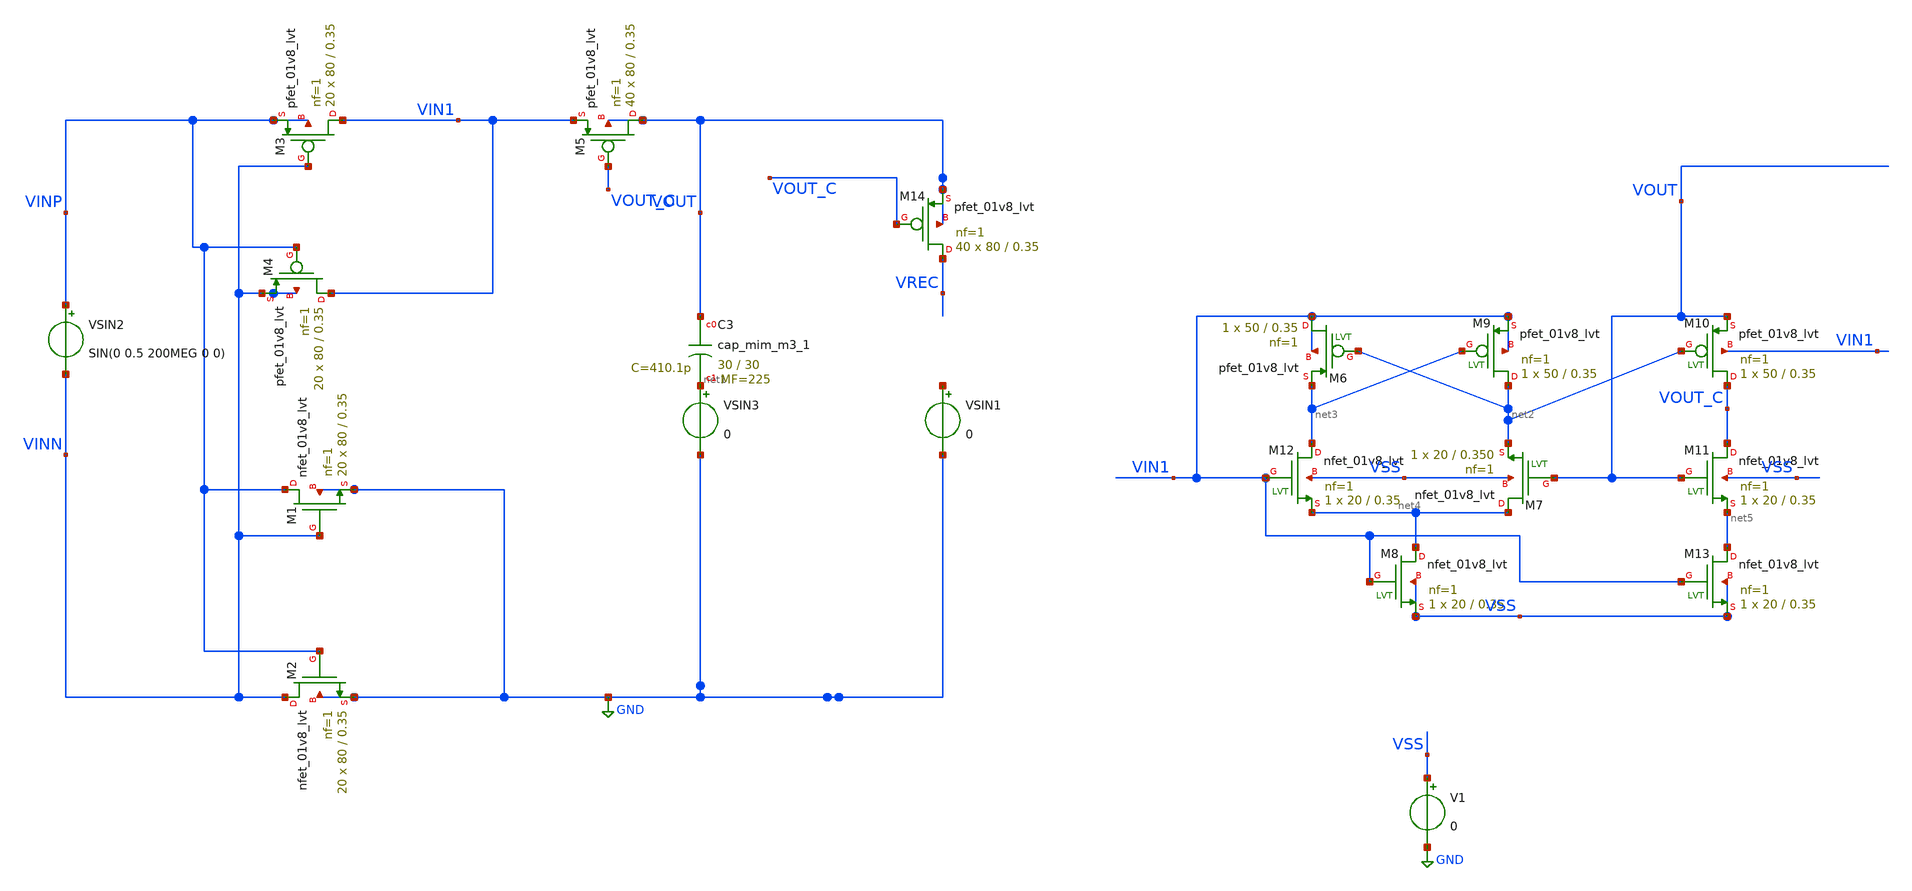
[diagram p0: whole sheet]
** sch_path: Schematics/PICOOAYOUT.sch
**.subckt PICOOAYOUT
XM1 VINP VINN GND GND sky130_fd_pr__nfet_01v8_lvt L=0.35 W=80 nf=1 ad='int((nf+1)/2) * W/nf * 0.29' as='int((nf+2)/2) * W/nf * 0.29'
+ pd='2*int((nf+1)/2) * (W/nf + 0.29)' ps='2*int((nf+2)/2) * (W/nf + 0.29)' nrd='0.29 / W' nrs='0.29 / W'
+ sa=0 sb=0 sd=0 mult=20 m=20
XM2 VINN VINP GND GND sky130_fd_pr__nfet_01v8_lvt L=0.35 W=80 nf=1 ad='int((nf+1)/2) * W/nf * 0.29' as='int((nf+2)/2) * W/nf * 0.29'
+ pd='2*int((nf+1)/2) * (W/nf + 0.29)' ps='2*int((nf+2)/2) * (W/nf + 0.29)' nrd='0.29 / W' nrs='0.29 / W'
+ sa=0 sb=0 sd=0 mult=20 m=20
XM4 VIN1 VINP VINN VINN sky130_fd_pr__pfet_01v8_lvt L=0.35 W=80 nf=1 ad='int((nf+1)/2) * W/nf * 0.29'
+ as='int((nf+2)/2) * W/nf * 0.29' pd='2*int((nf+1)/2) * (W/nf + 0.29)' ps='2*int((nf+2)/2) * (W/nf + 0.29)'
+ nrd='0.29 / W' nrs='0.29 / W' sa=0 sb=0 sd=0 mult=20 m=20
XM3 VIN1 VINN VINP VINP sky130_fd_pr__pfet_01v8_lvt L=0.35 W=80 nf=1 ad='int((nf+1)/2) * W/nf * 0.29'
+ as='int((nf+2)/2) * W/nf * 0.29' pd='2*int((nf+1)/2) * (W/nf + 0.29)' ps='2*int((nf+2)/2) * (W/nf + 0.29)'
+ nrd='0.29 / W' nrs='0.29 / W' sa=0 sb=0 sd=0 mult=20 m=20
VSIN2 VINP VINN SIN(0 0.5 200MEG 0 0)
XM5 VOUT VOUT_C VIN1 VOUT sky130_fd_pr__pfet_01v8_lvt L=0.35 W=80 nf=1 ad='int((nf+1)/2) * W/nf * 0.29'
+ as='int((nf+2)/2) * W/nf * 0.29' pd='2*int((nf+1)/2) * (W/nf + 0.29)' ps='2*int((nf+2)/2) * (W/nf + 0.29)'
+ nrd='0.29 / W' nrs='0.29 / W' sa=0 sb=0 sd=0 mult=40 m=40
XM6 VIN1 net2 net3 VIN1 sky130_fd_pr__pfet_01v8_lvt L=0.35 W=50 nf=1 ad='int((nf+1)/2) * W/nf * 0.29'
+ as='int((nf+2)/2) * W/nf * 0.29' pd='2*int((nf+1)/2) * (W/nf + 0.29)' ps='2*int((nf+2)/2) * (W/nf + 0.29)'
+ nrd='0.29 / W' nrs='0.29 / W' sa=0 sb=0 sd=0 mult=1 m=1
XM7 net4 VOUT net2 VSS sky130_fd_pr__nfet_01v8_lvt L=0.350 W=20 nf=1 ad='int((nf+1)/2) * W/nf * 0.29'
+ as='int((nf+2)/2) * W/nf * 0.29' pd='2*int((nf+1)/2) * (W/nf + 0.29)' ps='2*int((nf+2)/2) * (W/nf + 0.29)'
+ nrd='0.29 / W' nrs='0.29 / W' sa=0 sb=0 sd=0 mult=1 m=1
XM8 net4 VIN1 VSS VSS sky130_fd_pr__nfet_01v8_lvt L=0.35 W=20 nf=1 ad='int((nf+1)/2) * W/nf * 0.29' as='int((nf+2)/2) * W/nf * 0.29'
+ pd='2*int((nf+1)/2) * (W/nf + 0.29)' ps='2*int((nf+2)/2) * (W/nf + 0.29)' nrd='0.29 / W' nrs='0.29 / W'
+ sa=0 sb=0 sd=0 mult=1 m=1
XM9 net2 net3 VIN1 VIN1 sky130_fd_pr__pfet_01v8_lvt L=0.35 W=50 nf=1 ad='int((nf+1)/2) * W/nf * 0.29'
+ as='int((nf+2)/2) * W/nf * 0.29' pd='2*int((nf+1)/2) * (W/nf + 0.29)' ps='2*int((nf+2)/2) * (W/nf + 0.29)'
+ nrd='0.29 / W' nrs='0.29 / W' sa=0 sb=0 sd=0 mult=1 m=1
XM10 VOUT_C net2 VOUT VIN1 sky130_fd_pr__pfet_01v8_lvt L=0.35 W=50 nf=1 ad='int((nf+1)/2) * W/nf * 0.29'
+ as='int((nf+2)/2) * W/nf * 0.29' pd='2*int((nf+1)/2) * (W/nf + 0.29)' ps='2*int((nf+2)/2) * (W/nf + 0.29)'
+ nrd='0.29 / W' nrs='0.29 / W' sa=0 sb=0 sd=0 mult=1 m=1
XM11 VOUT_C VOUT net5 VSS sky130_fd_pr__nfet_01v8_lvt L=0.35 W=20 nf=1 ad='int((nf+1)/2) * W/nf * 0.29'
+ as='int((nf+2)/2) * W/nf * 0.29' pd='2*int((nf+1)/2) * (W/nf + 0.29)' ps='2*int((nf+2)/2) * (W/nf + 0.29)'
+ nrd='0.29 / W' nrs='0.29 / W' sa=0 sb=0 sd=0 mult=1 m=1
XM12 net3 VIN1 net4 VSS sky130_fd_pr__nfet_01v8_lvt L=0.35 W=20 nf=1 ad='int((nf+1)/2) * W/nf * 0.29'
+ as='int((nf+2)/2) * W/nf * 0.29' pd='2*int((nf+1)/2) * (W/nf + 0.29)' ps='2*int((nf+2)/2) * (W/nf + 0.29)'
+ nrd='0.29 / W' nrs='0.29 / W' sa=0 sb=0 sd=0 mult=1 m=1
XM13 net5 VIN1 VSS VSS sky130_fd_pr__nfet_01v8_lvt L=0.35 W=20 nf=1 ad='int((nf+1)/2) * W/nf * 0.29'
+ as='int((nf+2)/2) * W/nf * 0.29' pd='2*int((nf+1)/2) * (W/nf + 0.29)' ps='2*int((nf+2)/2) * (W/nf + 0.29)'
+ nrd='0.29 / W' nrs='0.29 / W' sa=0 sb=0 sd=0 mult=1 m=1
V1 VSS GND 0
VSIN1 net6 GND 0
VSIN3 net1 GND 0
XM14 VREC VOUT_C VOUT VOUT sky130_fd_pr__pfet_01v8_lvt L=0.35 W=80 nf=1 ad='int((nf+1)/2) * W/nf * 0.29'
+ as='int((nf+2)/2) * W/nf * 0.29' pd='2*int((nf+1)/2) * (W/nf + 0.29)' ps='2*int((nf+2)/2) * (W/nf + 0.29)'
+ nrd='0.29 / W' nrs='0.29 / W' sa=0 sb=0 sd=0 mult=40 m=40
XC3 VOUT net1 sky130_fd_pr__cap_mim_m3_1 W=30 L=30 MF=225 m=225
**** begin user architecture code


	.control
	save all
	tran 1ns 20us
	Let PIN1= AVG(VINP*(i(VSIN2)))
	Let PIN2= AVG(VINN*(i(VSIN2)))
	Let PIN=PIN2+PIN2
	Let POUT1= AVG(VOUT*(i(VSIN3)))
	Let POUT2= AVG(VOUT*(i(VSIN1)))
	Let POUT=POUT1+POUT2

	Let EFF=(POUT/PIN)

	*plot VOUT VIN1
	*plot PIN
	plot POUT
	plot VOUT
	*plot POUT1
	*plot POUT2
	plot EFF
	*plot VOUT_C
	plot VREC



	*plot POUT


.endc


 ** manual skywater pdks install (with patches applied)
* .lib $::SKYWATER_MODELS/models/sky130.lib.spice tt

** opencircuitdesign pdks install
.lib $::SKYWATER_MODELS/sky130.lib.spice tt

.param mc_mm_switch=0
.param mc_pr_switch=0

**** end user architecture code
**.ends
.GLOBAL GND
.end
